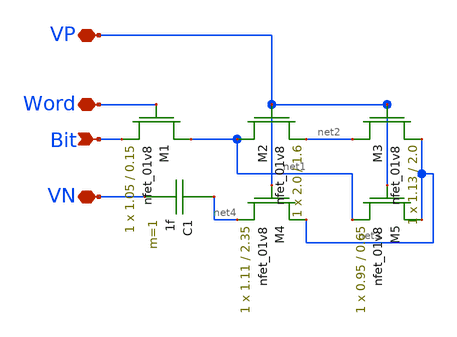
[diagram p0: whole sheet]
** sch_path: DRAM_Components/Schematic/MemoryCell2.sch
**.subckt MemoryCell2 Bit VP Word VN
*.ipin Bit
*.iopin VP
*.iopin Word
*.iopin VN
XM1 net1 Word Bit VN sky130_fd_pr__nfet_01v8 L=0.15 W=1.05 nf=1 ad='int((nf+1)/2) * W/nf * 0.29' as='int((nf+2)/2) * W/nf * 0.29'
+ pd='2*int((nf+1)/2) * (W/nf + 0.29)' ps='2*int((nf+2)/2) * (W/nf + 0.29)' nrd='0.29 / W' nrs='0.29 / W'
+ sa=0 sb=0 sd=0 mult=1 m=1
XM2 net1 VP net2 VN sky130_fd_pr__nfet_01v8 L=1.6 W=2.0 nf=1 ad='int((nf+1)/2) * W/nf * 0.29' as='int((nf+2)/2) * W/nf * 0.29'
+ pd='2*int((nf+1)/2) * (W/nf + 0.29)' ps='2*int((nf+2)/2) * (W/nf + 0.29)' nrd='0.29 / W' nrs='0.29 / W'
+ sa=0 sb=0 sd=0 mult=1 m=1
XM3 net2 VP net3 VN sky130_fd_pr__nfet_01v8 L=2.0 W=1.13 nf=1 ad='int((nf+1)/2) * W/nf * 0.29' as='int((nf+2)/2) * W/nf * 0.29'
+ pd='2*int((nf+1)/2) * (W/nf + 0.29)' ps='2*int((nf+2)/2) * (W/nf + 0.29)' nrd='0.29 / W' nrs='0.29 / W'
+ sa=0 sb=0 sd=0 mult=1 m=1
XM4 net3 VP net4 VN sky130_fd_pr__nfet_01v8 L=2.35 W=1.11 nf=1 ad='int((nf+1)/2) * W/nf * 0.29' as='int((nf+2)/2) * W/nf * 0.29'
+ pd='2*int((nf+1)/2) * (W/nf + 0.29)' ps='2*int((nf+2)/2) * (W/nf + 0.29)' nrd='0.29 / W' nrs='0.29 / W'
+ sa=0 sb=0 sd=0 mult=1 m=1
XM5 net3 VP net1 VN sky130_fd_pr__nfet_01v8 L=0.65 W=0.95 nf=1 ad='int((nf+1)/2) * W/nf * 0.29' as='int((nf+2)/2) * W/nf * 0.29'
+ pd='2*int((nf+1)/2) * (W/nf + 0.29)' ps='2*int((nf+2)/2) * (W/nf + 0.29)' nrd='0.29 / W' nrs='0.29 / W'
+ sa=0 sb=0 sd=0 mult=1 m=1
C1 net4 VN 1f m=1
**.ends
.end
